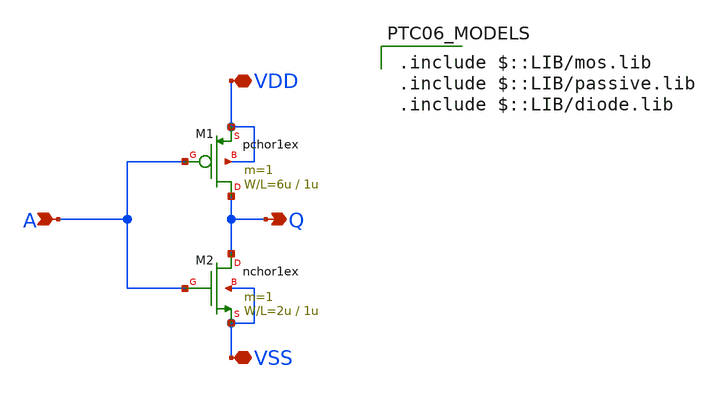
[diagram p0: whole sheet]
** sch_path: member_project/masahiro/myfirstlayout.sch
**.subckt myfirstlayout A Q VDD VSS
*.ipin A
*.opin Q
*.iopin VDD
*.iopin VSS
M1 Q A VDD VDD pchor1ex L=1u W=6u m=1
M2 Q A VSS VSS nchor1ex L=1u W=2u m=1
**** begin user architecture code
 .include $::LIB/mos.lib
.include $::LIB/passive.lib
.include $::LIB/diode.lib
**** end user architecture code
**.ends
.end
